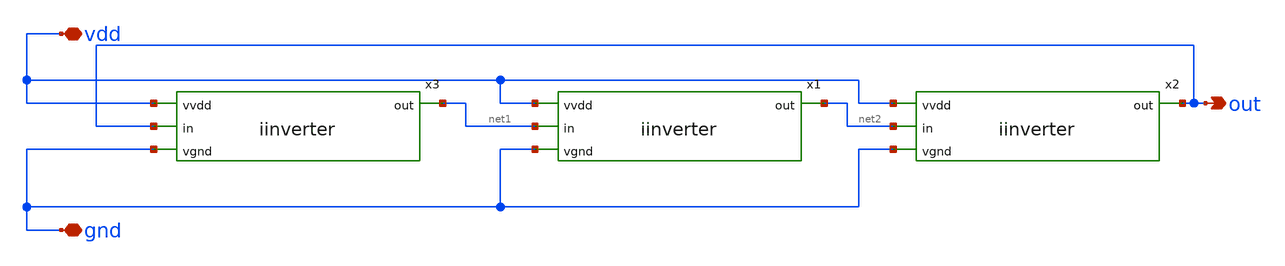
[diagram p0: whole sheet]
** sch_path: iinverter/ring_oscillator3.sch
**.subckt ring_oscillator3 vdd out gnd
*.iopin vdd
*.opin out
*.iopin gnd
x1 vdd net1 net2 gnd iinverter
x2 vdd net2 out gnd iinverter
x3 vdd out net1 gnd iinverter
**.ends

* expanding   symbol:  iinverter.sym # of pins=4
** sym_path: iinverter/iinverter.sym
** sch_path: iinverter/iinverter.sch
.subckt iinverter vvdd in out vgnd
*.ipin vvdd
*.ipin in
*.ipin vgnd
*.opin out
XM3 out in vgnd vgnd sky130_fd_pr__nfet_01v8 L=0.15 W=1 nf=1 ad='int((nf+1)/2) * W/nf * 0.29' as='int((nf+2)/2) * W/nf * 0.29'
+ pd='2*int((nf+1)/2) * (W/nf + 0.29)' ps='2*int((nf+2)/2) * (W/nf + 0.29)' nrd='0.29 / W' nrs='0.29 / W'
+ sa=0 sb=0 sd=0 mult=1 m=1
XM2 out in vvdd vvdd sky130_fd_pr__pfet_01v8 L=0.15 W=1 nf=1 ad='int((nf+1)/2) * W/nf * 0.29' as='int((nf+2)/2) * W/nf * 0.29'
+ pd='2*int((nf+1)/2) * (W/nf + 0.29)' ps='2*int((nf+2)/2) * (W/nf + 0.29)' nrd='0.29 / W' nrs='0.29 / W'
+ sa=0 sb=0 sd=0 mult=1 m=1
.ends

.end
